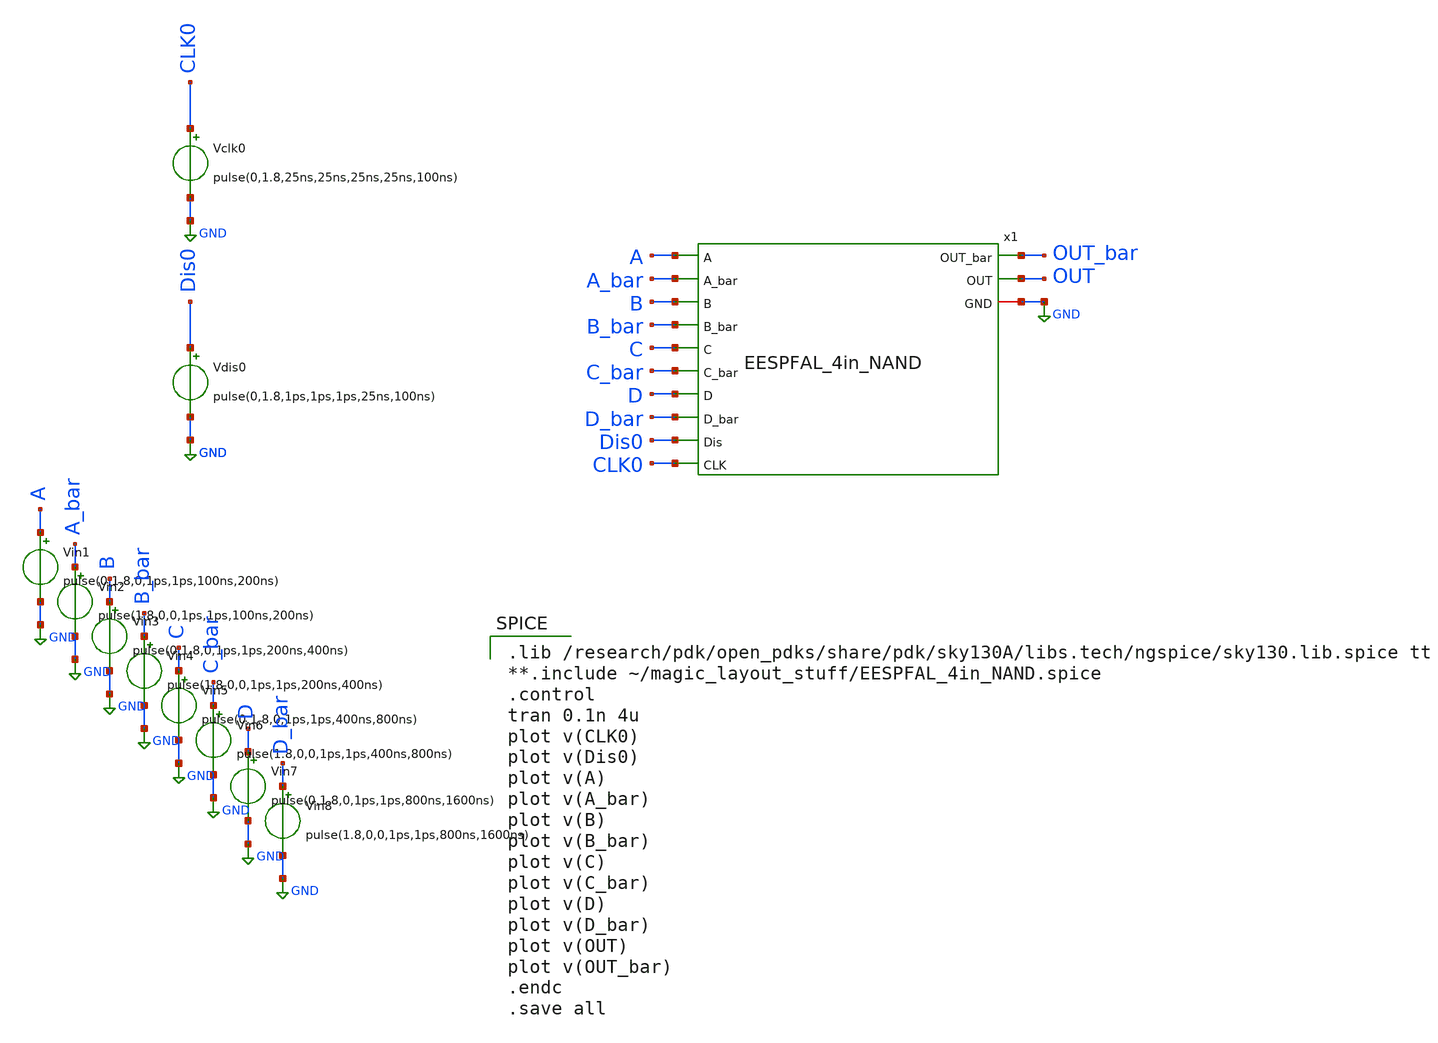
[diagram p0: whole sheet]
** sch_path: skywater_stuff/EESPFAL_4in_NAND_sim.sch
**.subckt EESPFAL_4in_NAND_sim
Vclk0 CLK0 GND pulse(0,1.8,25ns,25ns,25ns,25ns,100ns)
Vin1 A GND pulse(0,1.8,0,1ps,1ps,100ns,200ns)
Vin2 A_bar GND pulse(1.8,0,0,1ps,1ps,100ns,200ns)
Vdis0 Dis0 GND pulse(0,1.8,1ps,1ps,1ps,25ns,100ns)
Vin3 B GND pulse(0,1.8,0,1ps,1ps,200ns,400ns)
Vin4 B_bar GND pulse(1.8,0,0,1ps,1ps,200ns,400ns)
Vin5 C GND pulse(0,1.8,0,1ps,1ps,400ns,800ns)
Vin6 C_bar GND pulse(1.8,0,0,1ps,1ps,400ns,800ns)
Vin7 D GND pulse(0,1.8,0,1ps,1ps,800ns,1600ns)
Vin8 D_bar GND pulse(1.8,0,0,1ps,1ps,800ns,1600ns)
x1 A A_bar B B_bar C C_bar D D_bar OUT OUT_bar Dis0 GND CLK0 EESPFAL_4in_NAND
**** begin user architecture code

.lib /research/pdk/open_pdks/share/pdk/sky130A/libs.tech/ngspice/sky130.lib.spice tt
**.include ~/magic_layout_stuff/EESPFAL_4in_NAND.spice
.control
tran 0.1n 4u
plot v(CLK0)
plot v(Dis0)
plot v(A)
plot v(A_bar)
plot v(B)
plot v(B_bar)
plot v(C)
plot v(C_bar)
plot v(D)
plot v(D_bar)
plot v(OUT)
plot v(OUT_bar)
.endc
.save all

**** end user architecture code
**.ends

* expanding   symbol:  EESPFAL_4in_NAND.sym # of pins=13
** sym_path: skywater_stuff/EESPFAL_4in_NAND.sym
** sch_path: skywater_stuff/EESPFAL_4in_NAND.sch
.subckt EESPFAL_4in_NAND A A_bar B B_bar C C_bar D D_bar OUT OUT_bar Dis GND CLK
*.ipin A
*.ipin A_bar
*.ipin B
*.ipin B_bar
*.ipin C
*.ipin C_bar
*.ipin D
*.ipin D_bar
*.opin OUT
*.opin OUT_bar
*.ipin Dis
*.iopin GND
*.ipin CLK
XM2 OUT OUT_bar CLK CLK sky130_fd_pr__pfet_01v8 L=0.15 W=1.5 nf=1 ad='int((nf+1)/2) * W/nf * 0.29' as='int((nf+2)/2) * W/nf * 0.29'
+ pd='2*int((nf+1)/2) * (W/nf + 0.29)' ps='2*int((nf+2)/2) * (W/nf + 0.29)' nrd='0.29 / W' nrs='0.29 / W'
+ sa=0 sb=0 sd=0 mult=2 m=2
XM11 CLK B_bar OUT_bar GND sky130_fd_pr__nfet_01v8 L=0.15 W=1.5 nf=1 ad='int((nf+1)/2) * W/nf * 0.29'
+ as='int((nf+2)/2) * W/nf * 0.29' pd='2*int((nf+1)/2) * (W/nf + 0.29)' ps='2*int((nf+2)/2) * (W/nf + 0.29)'
+ nrd='0.29 / W' nrs='0.29 / W' sa=0 sb=0 sd=0 mult=1 m=1
XM7 CLK A_bar OUT_bar GND sky130_fd_pr__nfet_01v8 L=0.15 W=1.5 nf=1 ad='int((nf+1)/2) * W/nf * 0.29'
+ as='int((nf+2)/2) * W/nf * 0.29' pd='2*int((nf+1)/2) * (W/nf + 0.29)' ps='2*int((nf+2)/2) * (W/nf + 0.29)'
+ nrd='0.29 / W' nrs='0.29 / W' sa=0 sb=0 sd=0 mult=1 m=1
XM8 net1 B net2 GND sky130_fd_pr__nfet_01v8 L=0.15 W=1.5 nf=1 ad='int((nf+1)/2) * W/nf * 0.29' as='int((nf+2)/2) * W/nf * 0.29'
+ pd='2*int((nf+1)/2) * (W/nf + 0.29)' ps='2*int((nf+2)/2) * (W/nf + 0.29)' nrd='0.29 / W' nrs='0.29 / W'
+ sa=0 sb=0 sd=0 mult=1 m=1
XM1 OUT OUT_bar GND GND sky130_fd_pr__nfet_01v8 L=0.15 W=1.5 nf=1 ad='int((nf+1)/2) * W/nf * 0.29' as='int((nf+2)/2) * W/nf * 0.29'
+ pd='2*int((nf+1)/2) * (W/nf + 0.29)' ps='2*int((nf+2)/2) * (W/nf + 0.29)' nrd='0.29 / W' nrs='0.29 / W'
+ sa=0 sb=0 sd=0 mult=1 m=1
XM5 OUT Dis GND GND sky130_fd_pr__nfet_01v8 L=0.15 W=1.5 nf=1 ad='int((nf+1)/2) * W/nf * 0.29' as='int((nf+2)/2) * W/nf * 0.29'
+ pd='2*int((nf+1)/2) * (W/nf + 0.29)' ps='2*int((nf+2)/2) * (W/nf + 0.29)' nrd='0.29 / W' nrs='0.29 / W'
+ sa=0 sb=0 sd=0 mult=1 m=1
XM6 OUT_bar Dis GND GND sky130_fd_pr__nfet_01v8 L=0.15 W=1.5 nf=1 ad='int((nf+1)/2) * W/nf * 0.29' as='int((nf+2)/2) * W/nf * 0.29'
+ pd='2*int((nf+1)/2) * (W/nf + 0.29)' ps='2*int((nf+2)/2) * (W/nf + 0.29)' nrd='0.29 / W' nrs='0.29 / W'
+ sa=0 sb=0 sd=0 mult=1 m=1
XM10 CLK C_bar OUT_bar GND sky130_fd_pr__nfet_01v8 L=0.15 W=1.5 nf=1 ad='int((nf+1)/2) * W/nf * 0.29'
+ as='int((nf+2)/2) * W/nf * 0.29' pd='2*int((nf+1)/2) * (W/nf + 0.29)' ps='2*int((nf+2)/2) * (W/nf + 0.29)'
+ nrd='0.29 / W' nrs='0.29 / W' sa=0 sb=0 sd=0 mult=1 m=1
XM9 CLK A net1 GND sky130_fd_pr__nfet_01v8 L=0.15 W=1.5 nf=1 ad='int((nf+1)/2) * W/nf * 0.29' as='int((nf+2)/2) * W/nf * 0.29'
+ pd='2*int((nf+1)/2) * (W/nf + 0.29)' ps='2*int((nf+2)/2) * (W/nf + 0.29)' nrd='0.29 / W' nrs='0.29 / W'
+ sa=0 sb=0 sd=0 mult=1 m=1
XM12 net2 C net3 GND sky130_fd_pr__nfet_01v8 L=0.15 W=1.5 nf=1 ad='int((nf+1)/2) * W/nf * 0.29' as='int((nf+2)/2) * W/nf * 0.29'
+ pd='2*int((nf+1)/2) * (W/nf + 0.29)' ps='2*int((nf+2)/2) * (W/nf + 0.29)' nrd='0.29 / W' nrs='0.29 / W'
+ sa=0 sb=0 sd=0 mult=1 m=1
XM4 OUT_bar OUT CLK CLK sky130_fd_pr__pfet_01v8 L=0.15 W=1.5 nf=1 ad='int((nf+1)/2) * W/nf * 0.29' as='int((nf+2)/2) * W/nf * 0.29'
+ pd='2*int((nf+1)/2) * (W/nf + 0.29)' ps='2*int((nf+2)/2) * (W/nf + 0.29)' nrd='0.29 / W' nrs='0.29 / W'
+ sa=0 sb=0 sd=0 mult=2 m=2
XM13 CLK D_bar OUT_bar GND sky130_fd_pr__nfet_01v8 L=0.15 W=1.5 nf=1 ad='int((nf+1)/2) * W/nf * 0.29'
+ as='int((nf+2)/2) * W/nf * 0.29' pd='2*int((nf+1)/2) * (W/nf + 0.29)' ps='2*int((nf+2)/2) * (W/nf + 0.29)'
+ nrd='0.29 / W' nrs='0.29 / W' sa=0 sb=0 sd=0 mult=1 m=1
XM3 OUT_bar OUT GND GND sky130_fd_pr__nfet_01v8 L=0.15 W=1.5 nf=1 ad='int((nf+1)/2) * W/nf * 0.29' as='int((nf+2)/2) * W/nf * 0.29'
+ pd='2*int((nf+1)/2) * (W/nf + 0.29)' ps='2*int((nf+2)/2) * (W/nf + 0.29)' nrd='0.29 / W' nrs='0.29 / W'
+ sa=0 sb=0 sd=0 mult=1 m=1
XM14 net3 D OUT GND sky130_fd_pr__nfet_01v8 L=0.15 W=1.5 nf=1 ad='int((nf+1)/2) * W/nf * 0.29' as='int((nf+2)/2) * W/nf * 0.29'
+ pd='2*int((nf+1)/2) * (W/nf + 0.29)' ps='2*int((nf+2)/2) * (W/nf + 0.29)' nrd='0.29 / W' nrs='0.29 / W'
+ sa=0 sb=0 sd=0 mult=1 m=1
.ends

.GLOBAL GND
.end
